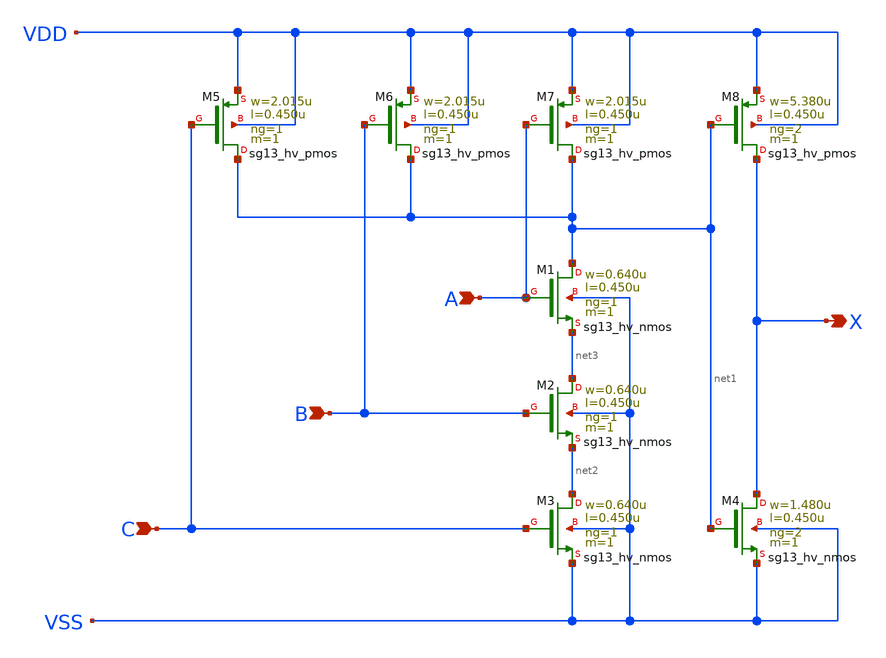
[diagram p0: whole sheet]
** sch_path: ihp-sg13g2/libs.ref/sg13g2_stdcell_hv/sch/xschem/sg13g2_hv_and3_2.sch
* Copyright 2023 IHP PDK Authors
* Licensed under the Apache License, Version 2.0 (the "License");
* you may not use this file except in compliance with the License.
* You may obtain a copy of the License at
* https://www.apache.org/licenses/LICENSE-2.0
* Unless required by applicable law or agreed to in writing, software
* distributed under the License is distributed on an "AS IS" BASIS,
* WITHOUT WARRANTIES OR CONDITIONS OF ANY KIND, either express or implied.
* See the License for the specific language governing permissions and
* limitations under the License.
**.subckt sg13g2_hv_and3_2 X C B A
*.opin X
*.ipin C
*.ipin B
*.ipin A
XM1 net1 A net3 VSS sg13_hv_nmos w=0.640u l=0.450u ng=1 m=1 mm_ok=1
XM2 net3 B net2 VSS sg13_hv_nmos w=0.640u l=0.450u ng=1 m=1 mm_ok=1
XM3 net2 C VSS VSS sg13_hv_nmos w=0.640u l=0.450u ng=1 m=1 mm_ok=1
XM4 X net1 VSS VSS sg13_hv_nmos w=1.480u l=0.450u ng=2 m=1 mm_ok=1
XM5 net1 C VDD VDD sg13_hv_pmos w=2.015u l=0.450u ng=1 m=1 mm_ok=1
XM6 net1 B VDD VDD sg13_hv_pmos w=2.015u l=0.450u ng=1 m=1 mm_ok=1
XM7 net1 A VDD VDD sg13_hv_pmos w=2.015u l=0.450u ng=1 m=1 mm_ok=1
XM8 X net1 VDD VDD sg13_hv_pmos w=5.380u l=0.450u ng=2 m=1 mm_ok=1
**.ends
.end
